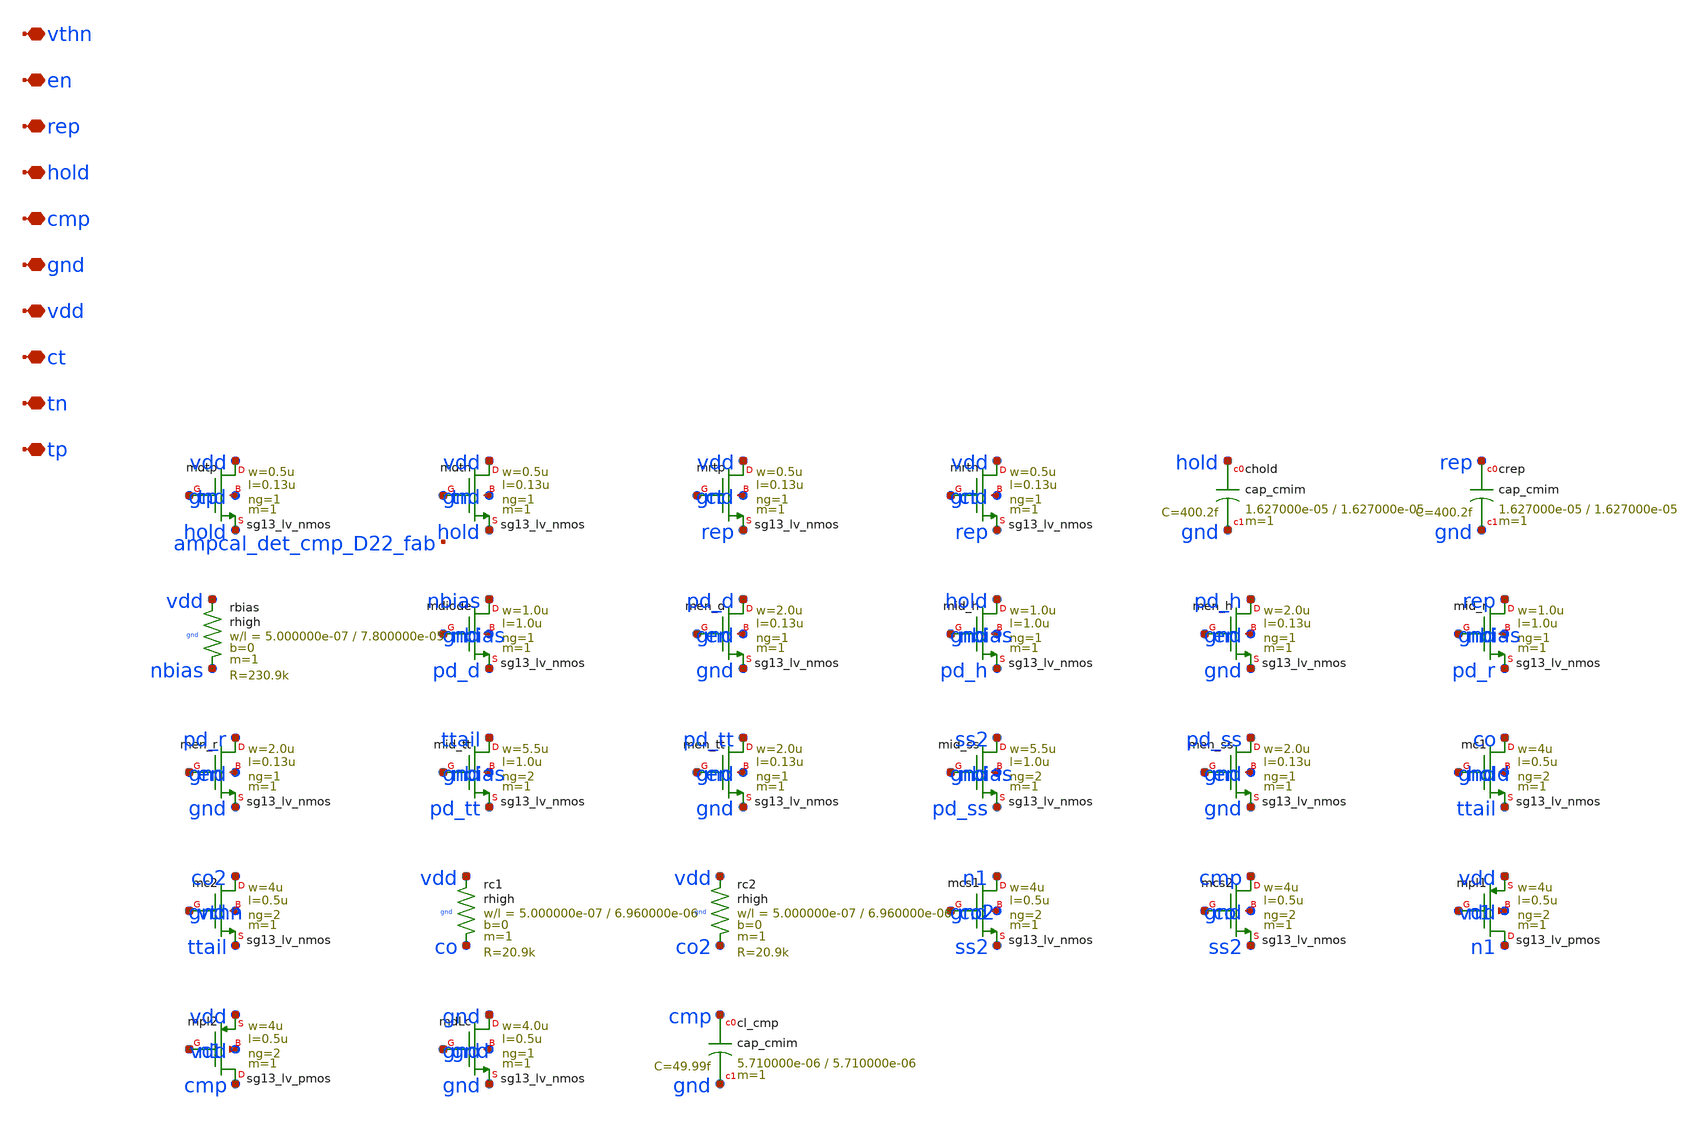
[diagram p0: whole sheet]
** sch_path: analog/vco/sch/ampcal_det.sch
**.subckt ampcal_det tp tn ct vdd gnd cmp hold rep en vthn
*.iopin tp
*.iopin tn
*.iopin ct
*.iopin vdd
*.iopin gnd
*.iopin cmp
*.iopin hold
*.iopin rep
*.iopin en
*.iopin vthn
Xmdtp vdd tp hold gnd sg13_lv_nmos w=0.5u l=0.13u ng=1 m=1 mm_ok=1
Xmdtn vdd tn hold gnd sg13_lv_nmos w=0.5u l=0.13u ng=1 m=1 mm_ok=1
Xmrtp vdd ct rep gnd sg13_lv_nmos w=0.5u l=0.13u ng=1 m=1 mm_ok=1
Xmrtn vdd ct rep gnd sg13_lv_nmos w=0.5u l=0.13u ng=1 m=1 mm_ok=1
Xchold hold gnd cap_cmim w=1.627000e-05 l=1.627000e-05 m=1 mm_ok=1
Xcrep rep gnd cap_cmim w=1.627000e-05 l=1.627000e-05 m=1 mm_ok=1
Xrbias vdd nbias gnd rhigh w=5.000000e-07 l=7.800000e-05 m=1 b=0 mm_ok=1
Xmdiode nbias nbias pd_d gnd sg13_lv_nmos w=1.0u l=1.0u ng=1 m=1 mm_ok=1
Xmen_d pd_d en gnd gnd sg13_lv_nmos w=2.0u l=0.13u ng=1 m=1 mm_ok=1
Xmid_h hold nbias pd_h gnd sg13_lv_nmos w=1.0u l=1.0u ng=1 m=1 mm_ok=1
Xmen_h pd_h en gnd gnd sg13_lv_nmos w=2.0u l=0.13u ng=1 m=1 mm_ok=1
Xmid_r rep nbias pd_r gnd sg13_lv_nmos w=1.0u l=1.0u ng=1 m=1 mm_ok=1
Xmen_r pd_r en gnd gnd sg13_lv_nmos w=2.0u l=0.13u ng=1 m=1 mm_ok=1
Xmid_tt ttail nbias pd_tt gnd sg13_lv_nmos w=5.5u l=1.0u ng=2 m=1 mm_ok=1
Xmen_tt pd_tt en gnd gnd sg13_lv_nmos w=2.0u l=0.13u ng=1 m=1 mm_ok=1
Xmid_ss ss2 nbias pd_ss gnd sg13_lv_nmos w=5.5u l=1.0u ng=2 m=1 mm_ok=1
Xmen_ss pd_ss en gnd gnd sg13_lv_nmos w=2.0u l=0.13u ng=1 m=1 mm_ok=1
Xmc1 co hold ttail gnd sg13_lv_nmos w=4u l=0.5u ng=2 m=1 mm_ok=1
Xmc2 co2 vthn ttail gnd sg13_lv_nmos w=4u l=0.5u ng=2 m=1 mm_ok=1
Xrc1 vdd co gnd rhigh w=5.000000e-07 l=6.960000e-06 m=1 b=0 mm_ok=1
Xrc2 vdd co2 gnd rhigh w=5.000000e-07 l=6.960000e-06 m=1 b=0 mm_ok=1
Xmcs1 n1 co2 ss2 gnd sg13_lv_nmos w=4u l=0.5u ng=2 m=1 mm_ok=1
Xmcs2 cmp co ss2 gnd sg13_lv_nmos w=4u l=0.5u ng=2 m=1 mm_ok=1
Xmpl1 n1 n1 vdd vdd sg13_lv_pmos w=4u l=0.5u ng=2 m=1 mm_ok=1
Xmpl2 cmp n1 vdd vdd sg13_lv_pmos w=4u l=0.5u ng=2 m=1 mm_ok=1
XmdLc gnd gnd gnd gnd sg13_lv_nmos w=4.0u l=0.5u ng=1 m=1 mm_ok=1
Xcl_cmp cmp gnd cap_cmim w=5.710000e-06 l=5.710000e-06 m=1 mm_ok=1
**.ends
.end
